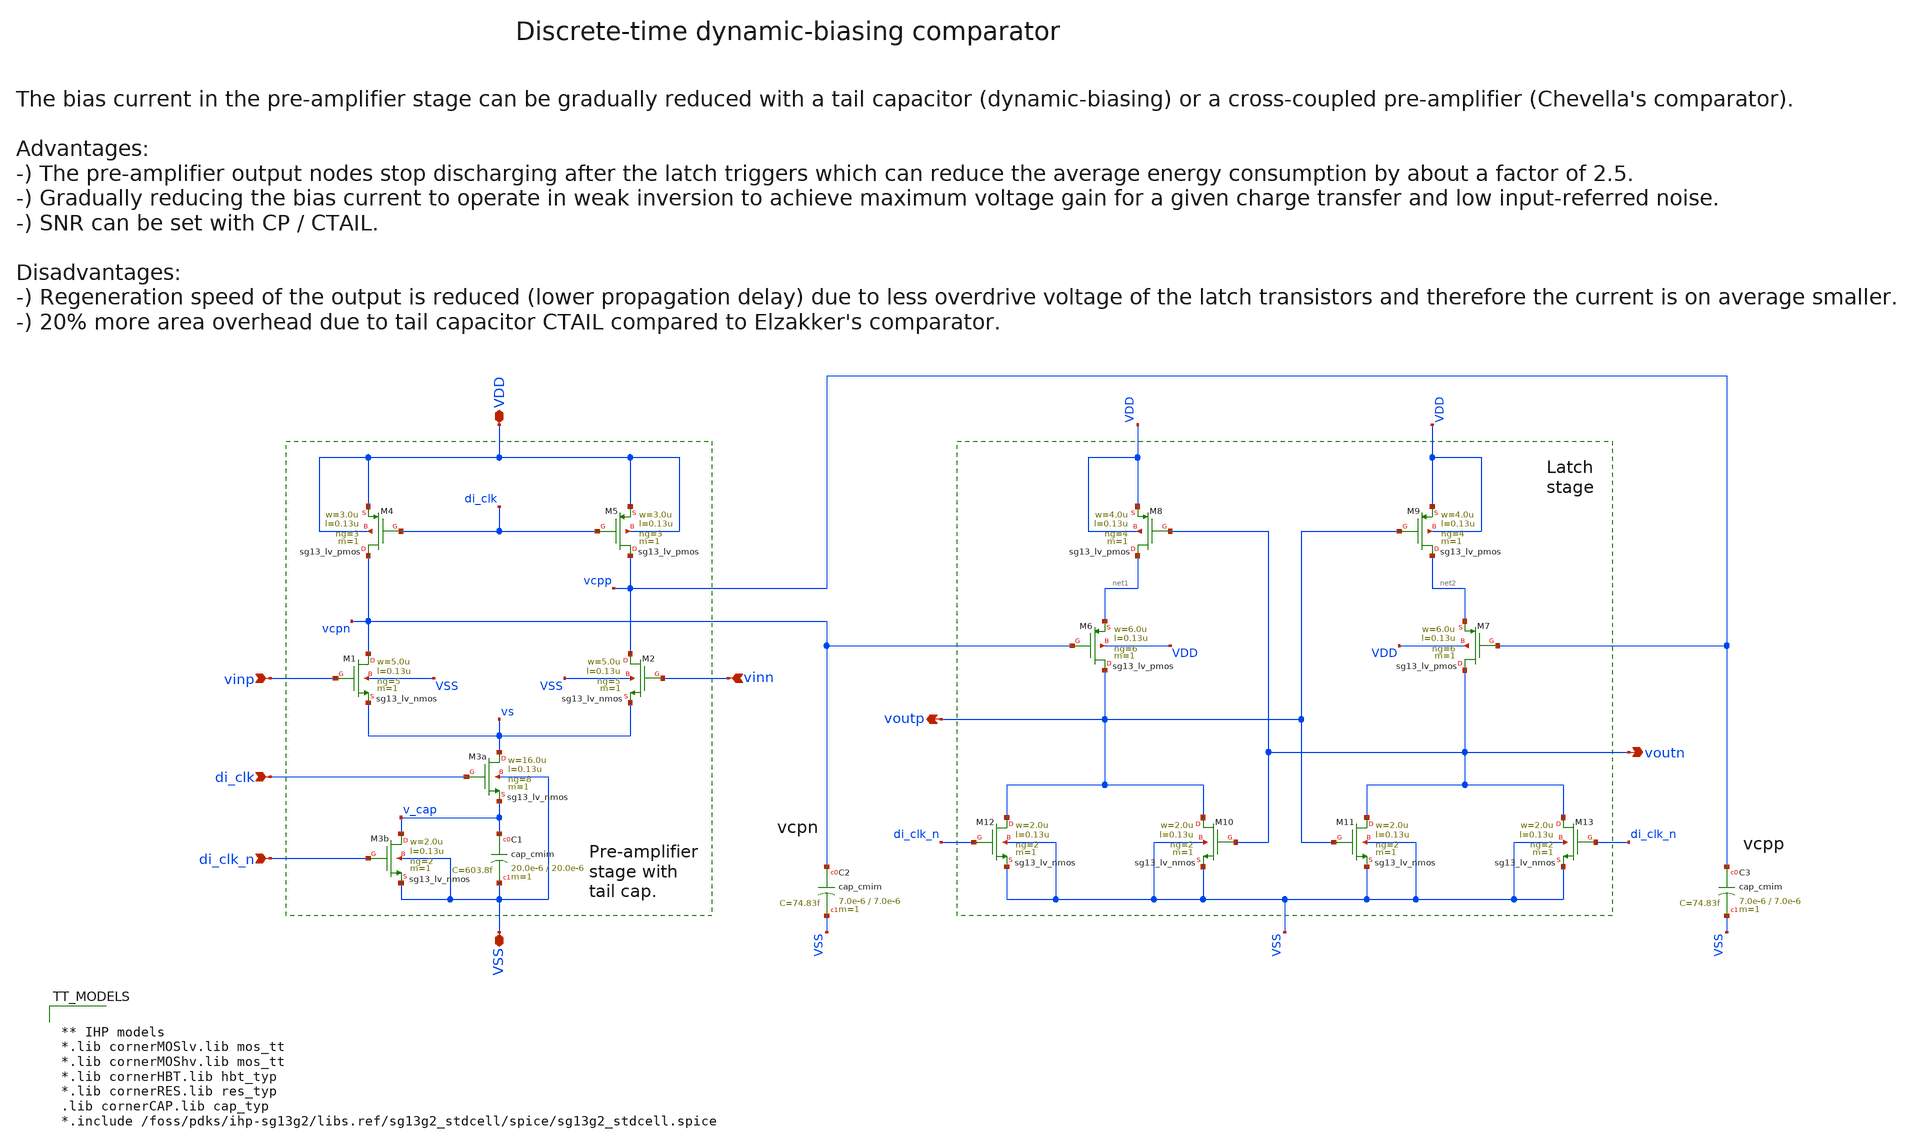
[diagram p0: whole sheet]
** sch_path: xschem/comparator/discrete_time/Dynamic-biasing/dynamic_biasing_comparator.sch
**.subckt dynamic_biasing_comparator VDD voutp voutn di_clk_n VSS vinp vinn di_clk
*.iopin VDD
*.opin voutp
*.opin voutn
*.ipin di_clk_n
*.iopin VSS
*.ipin vinp
*.ipin vinn
*.ipin di_clk
XM3a vs di_clk v_cap VSS sg13_lv_nmos w=16.0u l=0.13u ng=8 m=1 mm_ok=1
XM12 voutp di_clk_n VSS VSS sg13_lv_nmos w=2.0u l=0.13u ng=2 m=1 mm_ok=1
XM8 net1 voutn VDD VDD sg13_lv_pmos w=4.0u l=0.13u ng=4 m=1 mm_ok=1
XM10 voutp voutn VSS VSS sg13_lv_nmos w=2.0u l=0.13u ng=2 m=1 mm_ok=1
XM11 voutn voutp VSS VSS sg13_lv_nmos w=2.0u l=0.13u ng=2 m=1 mm_ok=1
XM13 voutn di_clk_n VSS VSS sg13_lv_nmos w=2.0u l=0.13u ng=2 m=1 mm_ok=1
XM9 net2 voutp VDD VDD sg13_lv_pmos w=4.0u l=0.13u ng=4 m=1 mm_ok=1
XM6 voutp vcpn net1 VDD sg13_lv_pmos w=6.0u l=0.13u ng=6 m=1 mm_ok=1
XM7 voutn vcpp net2 VDD sg13_lv_pmos w=6.0u l=0.13u ng=6 m=1 mm_ok=1
XM3b v_cap di_clk_n VSS VSS sg13_lv_nmos w=2.0u l=0.13u ng=2 m=1 mm_ok=1
XM1 vcpn vinp vs VSS sg13_lv_nmos w=5.0u l=0.13u ng=5 m=1 mm_ok=1
XM2 vcpp vinn vs VSS sg13_lv_nmos w=5.0u l=0.13u ng=5 m=1 mm_ok=1
XM4 vcpn di_clk VDD VDD sg13_lv_pmos w=3.0u l=0.13u ng=3 m=1 mm_ok=1
XM5 vcpp di_clk VDD VDD sg13_lv_pmos w=3.0u l=0.13u ng=3 m=1 mm_ok=1
XC1 v_cap VSS cap_cmim w=20.0e-6 l=20.0e-6 m=1 mm_ok=1
XC2 vcpn VSS cap_cmim w=7.0e-6 l=7.0e-6 m=1 mm_ok=1
XC3 vcpp VSS cap_cmim w=7.0e-6 l=7.0e-6 m=1 mm_ok=1
**** begin user architecture code


** IHP models
*.lib cornerMOSlv.lib mos_tt
*.lib cornerMOShv.lib mos_tt
*.lib cornerHBT.lib hbt_typ
*.lib cornerRES.lib res_typ
.lib cornerCAP.lib cap_typ
*.include /foss/pdks/ihp-sg13g2/libs.ref/sg13g2_stdcell/spice/sg13g2_stdcell.spice


**** end user architecture code
**.ends
.end
